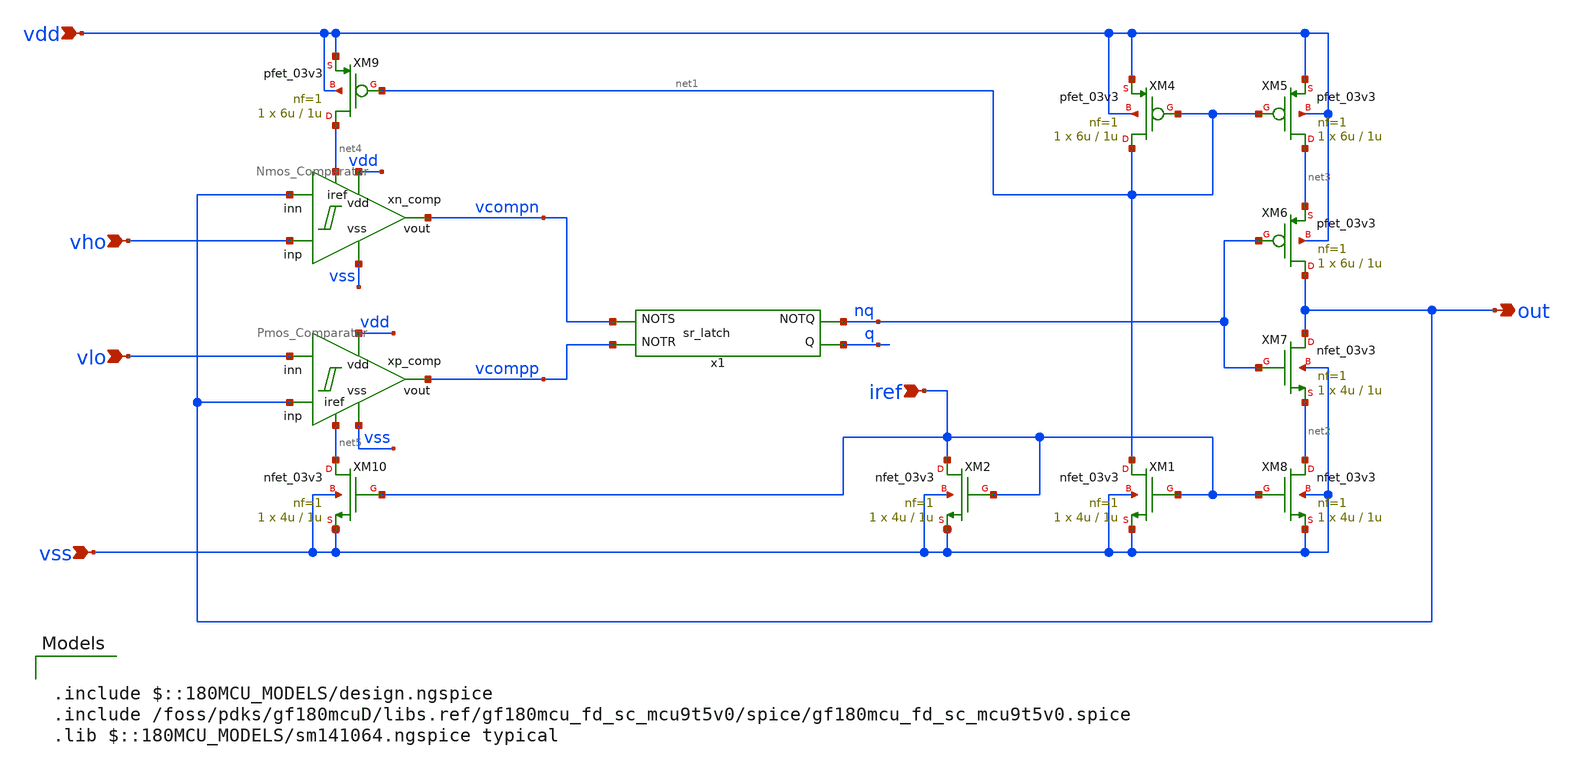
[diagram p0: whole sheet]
** sch_path: designs/switch_matrix_gf180mcu_9t5v0-main/designs/libs/core_analog/oscillator/triangle_osc.sch
**.subckt triangle_osc iref vss vho vlo out vdd
*.ipin iref
*.ipin vss
*.ipin vho
*.ipin vlo
*.opin out
*.ipin vdd
XM1 net1 iref vss vss nfet_03v3 L=1u W=4u nf=1 ad='int((nf+1)/2) * W/nf * 0.18u' as='int((nf+2)/2) * W/nf * 0.18u'
+ pd='2*int((nf+1)/2) * (W/nf + 0.18u)' ps='2*int((nf+2)/2) * (W/nf + 0.18u)' nrd='0.18u / W' nrs='0.18u / W'
+ sa=0 sb=0 sd=0 m=1
XM8 net2 iref vss vss nfet_03v3 L=1u W=4u nf=1 ad='int((nf+1)/2) * W/nf * 0.18u' as='int((nf+2)/2) * W/nf * 0.18u'
+ pd='2*int((nf+1)/2) * (W/nf + 0.18u)' ps='2*int((nf+2)/2) * (W/nf + 0.18u)' nrd='0.18u / W' nrs='0.18u / W'
+ sa=0 sb=0 sd=0 m=1
XM4 net1 net1 vdd vdd pfet_03v3 L=1u W=6u nf=1 ad='int((nf+1)/2) * W/nf * 0.18u' as='int((nf+2)/2) * W/nf * 0.18u'
+ pd='2*int((nf+1)/2) * (W/nf + 0.18u)' ps='2*int((nf+2)/2) * (W/nf + 0.18u)' nrd='0.18u / W' nrs='0.18u / W'
+ sa=0 sb=0 sd=0 m=1
XM5 net3 net1 vdd vdd pfet_03v3 L=1u W=6u nf=1 ad='int((nf+1)/2) * W/nf * 0.18u' as='int((nf+2)/2) * W/nf * 0.18u'
+ pd='2*int((nf+1)/2) * (W/nf + 0.18u)' ps='2*int((nf+2)/2) * (W/nf + 0.18u)' nrd='0.18u / W' nrs='0.18u / W'
+ sa=0 sb=0 sd=0 m=1
XM6 out nq net3 vdd pfet_03v3 L=1u W=6u nf=1 ad='int((nf+1)/2) * W/nf * 0.18u' as='int((nf+2)/2) * W/nf * 0.18u'
+ pd='2*int((nf+1)/2) * (W/nf + 0.18u)' ps='2*int((nf+2)/2) * (W/nf + 0.18u)' nrd='0.18u / W' nrs='0.18u / W'
+ sa=0 sb=0 sd=0 m=1
XM7 out nq net2 vss nfet_03v3 L=1u W=4u nf=1 ad='int((nf+1)/2) * W/nf * 0.18u' as='int((nf+2)/2) * W/nf * 0.18u'
+ pd='2*int((nf+1)/2) * (W/nf + 0.18u)' ps='2*int((nf+2)/2) * (W/nf + 0.18u)' nrd='0.18u / W' nrs='0.18u / W'
+ sa=0 sb=0 sd=0 m=1
XM2 iref iref vss vss nfet_03v3 L=1u W=4u nf=1 ad='int((nf+1)/2) * W/nf * 0.18u' as='int((nf+2)/2) * W/nf * 0.18u'
+ pd='2*int((nf+1)/2) * (W/nf + 0.18u)' ps='2*int((nf+2)/2) * (W/nf + 0.18u)' nrd='0.18u / W' nrs='0.18u / W'
+ sa=0 sb=0 sd=0 m=1
XM10 net5 iref vss vss nfet_03v3 L=1u W=4u nf=1 ad='int((nf+1)/2) * W/nf * 0.18u' as='int((nf+2)/2) * W/nf * 0.18u'
+ pd='2*int((nf+1)/2) * (W/nf + 0.18u)' ps='2*int((nf+2)/2) * (W/nf + 0.18u)' nrd='0.18u / W' nrs='0.18u / W'
+ sa=0 sb=0 sd=0 m=1
XM9 net4 net1 vdd vdd pfet_03v3 L=1u W=6u nf=1 ad='int((nf+1)/2) * W/nf * 0.18u' as='int((nf+2)/2) * W/nf * 0.18u'
+ pd='2*int((nf+1)/2) * (W/nf + 0.18u)' ps='2*int((nf+2)/2) * (W/nf + 0.18u)' nrd='0.18u / W' nrs='0.18u / W'
+ sa=0 sb=0 sd=0 m=1
xn_comp vdd vcompn vho vss out net4 Nmos_Comparator
xp_comp vdd vcompp out vss vlo net5 Pmos_Comparator
x1 vcompp q nq vcompn sr_latch
**** begin user architecture code

.include $::180MCU_MODELS/design.ngspice
.include /foss/pdks/gf180mcuD/libs.ref/gf180mcu_fd_sc_mcu9t5v0/spice/gf180mcu_fd_sc_mcu9t5v0.spice
.lib $::180MCU_MODELS/sm141064.ngspice typical

**** end user architecture code
**.ends
.end
